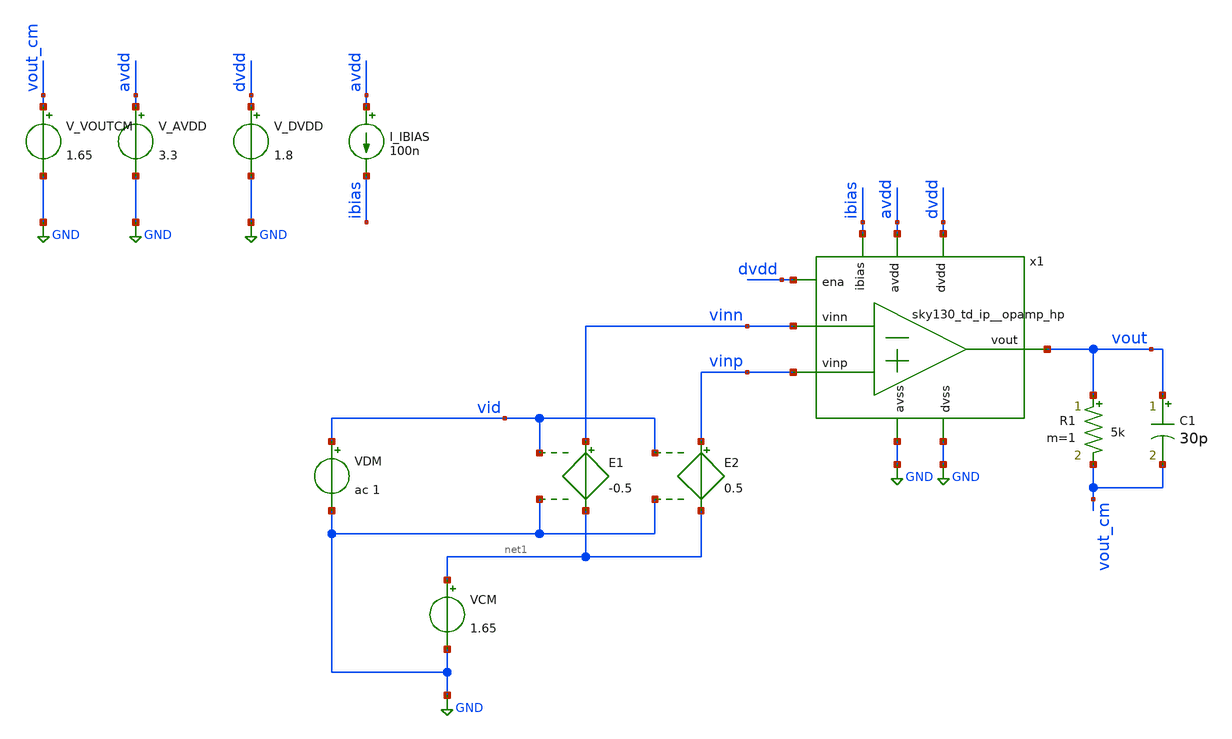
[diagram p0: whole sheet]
** sch_path: xschem/sky130_td_ip__opamp_hp_tb_ac.sch
**.subckt sky130_td_ip__opamp_hp_tb_ac
x1 avdd vout ibias vinn vinp GND dvdd GND dvdd sky130_td_ip__opamp_hp
V_AVDD avdd GND 3.3
.save i(v_avdd)
V_DVDD dvdd GND 1.8
.save i(v_dvdd)
I_IBIAS avdd ibias 100n
VCM net1 GND 1.65
R1 vout vout_cm 5k m=1
C1 vout vout_cm 30p m=1
V_VOUTCM vout_cm GND 1.65
.save i(v_voutcm)
E1 vinn net1 vid GND -0.5
VDM vid GND ac 1
E2 vinp net1 vid GND 0.5
**** begin user architecture code


.save all

.control
save all
AC DEC 100 1 1000000000
run

plot db(vout / vid)

.endc




.lib /usr/local/share/pdk/sky130A/libs.tech/combined/sky130.lib.spice tt


**** end user architecture code
**.ends
.GLOBAL GND
.end
